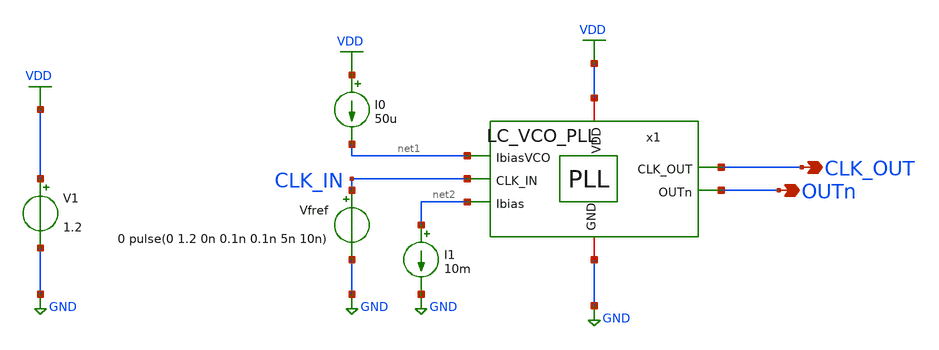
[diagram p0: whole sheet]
** sch_path: schematic/top-pll/LC_VCO_PLL_op_tb.sch
**.subckt LC_VCO_PLL_op_tb OUTn CLK_OUT
*.opin OUTn
*.opin CLK_OUT
V1 VDD GND 1.2
I0 VDD net1 50u
Vfref CLK_IN GND 0 pulse(0 1.2 0n 0.1n 0.1n 5n 10n)
I1 net2 GND 10m
x1 VDD CLK_IN CLK_OUT net1 OUTn net2 GND LC_VCO_PLL
**** begin user architecture code



*****************************************************
* PLL + DSM Frequency Divider Testbench
*****************************************************

.option temp = 27
.param VDD = 1.2

* ==============================
* Include Models
* ==============================

* Inductor / analog models
.include ./IHP_4nH_Inductor.spice

.control
save all
op
set filetype=ascii
write op_out.raw
print all > op_out.txt
.endc

* to generate following file copy stimuli.test
* to the simulation directory and run simulation -> Utile Stimuli Editor (GUI),
* and press 'Translate'
.include stimuli_test.cir






.lib cornerMOSlv.lib mos_tt
.lib cornerHBT.lib hbt_typ
.lib cornerRES.lib res_typ
.lib cornerCAP.lib cap_typ_stat
.include /foss/pdks/ihp-sg13g2/libs.ref/sg13g2_stdcell/spice/sg13g2_stdcell.spice
.global VDD GND


.param CP_N_L = 0.5u
.param CP_N_W = 10u
.param CP_P_M = 1
.param CP_P_L = 0.5u
.param CP_P_W = 30u
.param CP_N_M = 1
.param C_CP = 400p



**** end user architecture code
**.ends
.GLOBAL GND
.GLOBAL VDD
.end
